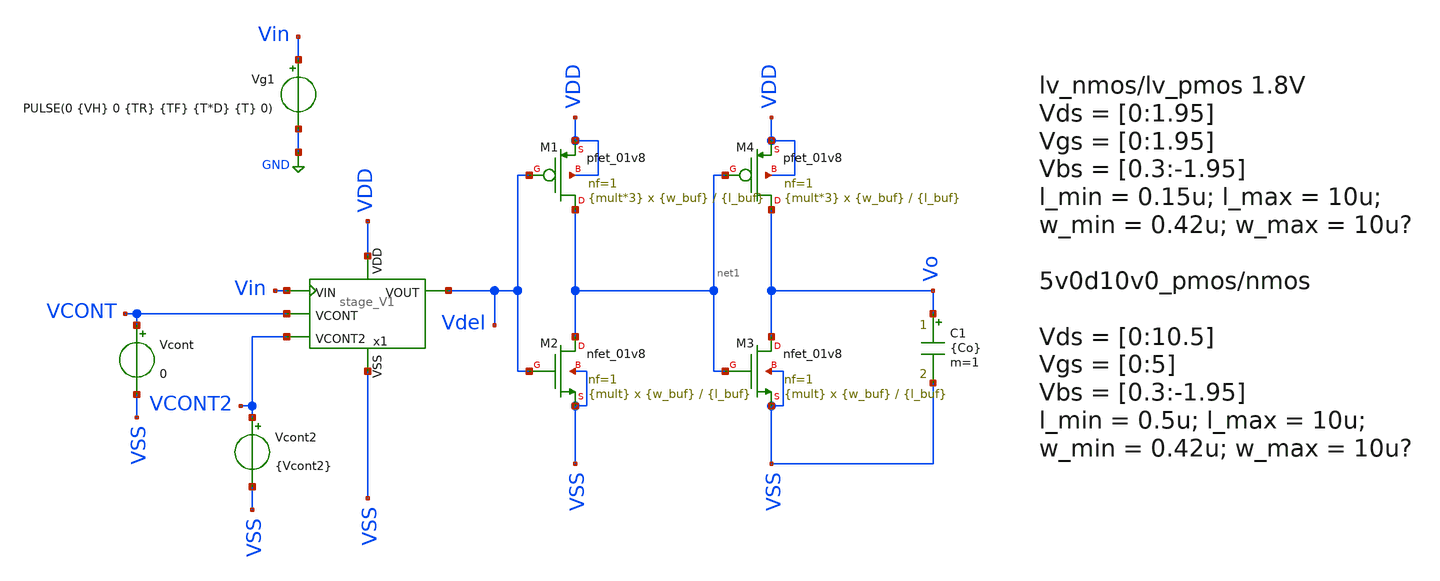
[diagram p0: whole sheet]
** sch_path: xschem/VCO/TB_DelCell_V1.sch
**.subckt TB_DelCell_V1
C1 Vo VSS {Co} m=1
Vcont VCONT VSS 0
Vg1 Vin GND PULSE(0 {VH} 0 {TR} {TF} {T*D} {T} 0)
XM2 net1 Vdel VSS VSS sky130_fd_pr__nfet_01v8 L={l_buf} W={w_buf} nf=1 ad='int((nf+1)/2) * W/nf * 0.29'
+ as='int((nf+2)/2) * W/nf * 0.29' pd='2*int((nf+1)/2) * (W/nf + 0.29)' ps='2*int((nf+2)/2) * (W/nf + 0.29)'
+ nrd='0.29 / W' nrs='0.29 / W' sa=0 sb=0 sd=0 mult={mult} m={mult}
XM1 net1 Vdel VDD VDD sky130_fd_pr__pfet_01v8 L={l_buf} W={w_buf} nf=1 ad='int((nf+1)/2) * W/nf * 0.29'
+ as='int((nf+2)/2) * W/nf * 0.29' pd='2*int((nf+1)/2) * (W/nf + 0.29)' ps='2*int((nf+2)/2) * (W/nf + 0.29)'
+ nrd='0.29 / W' nrs='0.29 / W' sa=0 sb=0 sd=0 mult={mult*3} m={mult*3}
XM3 Vo net1 VSS VSS sky130_fd_pr__nfet_01v8 L={l_buf} W={w_buf} nf=1 ad='int((nf+1)/2) * W/nf * 0.29'
+ as='int((nf+2)/2) * W/nf * 0.29' pd='2*int((nf+1)/2) * (W/nf + 0.29)' ps='2*int((nf+2)/2) * (W/nf + 0.29)'
+ nrd='0.29 / W' nrs='0.29 / W' sa=0 sb=0 sd=0 mult={mult} m={mult}
XM4 Vo net1 VDD VDD sky130_fd_pr__pfet_01v8 L={l_buf} W={w_buf} nf=1 ad='int((nf+1)/2) * W/nf * 0.29'
+ as='int((nf+2)/2) * W/nf * 0.29' pd='2*int((nf+1)/2) * (W/nf + 0.29)' ps='2*int((nf+2)/2) * (W/nf + 0.29)'
+ nrd='0.29 / W' nrs='0.29 / W' sa=0 sb=0 sd=0 mult={mult*3} m={mult*3}
x1 VDD VCONT Vdel Vin VSS VCONT2 stage_V1
Vcont2 VCONT2 VSS {Vcont2}
**** begin user architecture code

.lib /opt/pdks/sky130A/libs.tech/ngspice/sky130.lib.spice tt
*.lib /opt/pdks/sky130A/libs.tech/ngspice/sky130.lib.spice ss
*.lib /opt/pdks/sky130A/libs.tech/ngspice/sky130.lib.spice ff
*.lib /opt/pdks/sky130A/libs.tech/ngspice/sky130.lib.spice sf
*.lib /opt/pdks/sky130A/libs.tech/ngspice/sky130.lib.spice fs


.param Co = 0.1p
*.param Co = 0.1p
.param mult = 1
.param w_buf = 1
.param l_buf = 0.15

.param vvcont = 0
.param Vcont2 = 0.5

vvdd vdd 0 dc 1.8
vvss vss 0 0
*vvcont VCONT 0 dc 0
*vvcont2 VCONT2 0 dc 0
*.option temp = 200
.ic v(V_1) = 0
.ic v(V_2) = 1.8
.save v(V_1) v(Vo)


.param VH = 1.8

.ic v(Vo) = 0

*.param fsw = 10Meg
*.param fsw = 8.4Meg
*.param fsw = 1Meg
.param fsw = 50k

.param T = 1/fsw

.param D = 0.5
.param TR = 1n
.param TF = 1n
.param TdR = 0.5n
.param TdF = 0.5n

.param SimTime =  30*T
.csparam SimTime ={Simtime}
.csparam Tmargin = 10u





.save all
.tran 5n {SimTime}
.control
let Vtarg = 0.9

compose Vcont_sweep start = 0 stop = 1 step =0.1

let strt = 0
let stp = 1
let step = 0.1
let len = 1 + (stp-strt)/step

let VCN_sweep = vector(len)
let VCP_sweep = vector(len)
let Icont_sweep = vector(len)
let Iout_sweep = vector(len)
let Tdel_Sweep = vector(len)

let Index = 0

foreach val $&Vcont_sweep
	run
	alter vcont $val
	let Vo = v(Vo)
	let VCN_tran = v(x1.VCN)
	let VCP_tran = v(x1.VCP)
	let Icont_tran = i(v.x1.VIcont)
	let Iout_tran = i(v.x1.VIp)
	let In_tran  = i(v.x1.VIn)

	meas tran VCN AVG VCN_tran FROM=0 TO={SimTime}
	meas tran VCP AVG VCP_tran FROM=0 TO={SimTime}
	meas tran Icont AVG Icont_tran FROM=0 TO={SimTime}
	meas tran Iout AVG Iout_tran FROM=0 TO={SimTime}

	meas tran Tdel TRIG Vin VAL = {Vtarg} RISE = 20 TARG v(Vdel) VAL = {Vtarg}  RISE = 20

	*plot Vo Vin
	*plot VCN_tran VCP_tran
	*plot Icont_tran
	*plot Iout_tran
	print VCN VCP Icont Iout

	let VCN_sweep[index] = VCN
	let VCP_sweep[index] = VCP
	let Icont_sweep[index] = Icont
	let Iout_sweep[index] = Iout
	let Tdel_sweep[index] = Tdel
	let index = index +1
end

plot Icont_sweep vs Vcont_sweep
plot Iout_sweep vs VCP_sweep
plot Iout_sweep vs Vcont_sweep
plot VCP_sweep vs Vcont_sweep
plot Tdel_sweep vs Vcont_sweep
print VCN_sweep VCP_sweep Icont_sweep Iout_sweep Tdel_sweep

.endc




.param w_MP1a = 0.5
.param l_MP1a = 10
.param w_MP1b = 3.5
.param l_MP1b = 7
.param w_MP1 = 0.5
.param l_MP1 = 10
.param w_MP2 = 8
.param l_MP2 = 4
.param w_MP3 = 5
.param l_MP3 = 4
.param w_MP4 = 5
.param l_MP4 = 5

.param w_MN1 = 5
.param l_MN1 = 0.5
.param w_MN2 = 5
.param l_MN2 = 0.5
.param w_MN3 = 3
.param l_MN3 = 0.5
.param w_MN4 = 2
.param l_MN4 = 5



**** end user architecture code
**.ends

* expanding   symbol:  ../VCO/stage_V1.sym # of pins=6
** sym_path: xschem/VCO/stage_V1.sym
** sch_path: xschem/VCO/stage_V1.sch
.subckt stage_V1 VDD VCONT VOUT VIN VSS VCONT2
*.ipin VCONT2
*.ipin VIN
*.opin VOUT
*.iopin VDD
*.iopin VSS
*.ipin VCONT
XMN1 VSS net2 net2 VSS sg13_hv_nmos w={w_MN1} l={l_MN1} ng=1 m={m_MN1} mm_ok=1
XMN2 VSS net2 net3 VSS sg13_hv_nmos w={w_MN2} l={l_MN2} ng=1 m={m_MN2} mm_ok=1
XMN3 VSS net2 VdsMN3 VSS sg13_hv_nmos w={w_MN3} l={l_MN3} ng=1 m={m_MN3} mm_ok=1
XMP1a VCN VCONT VDD VDD sg13_hv_pmos w={w_MP1a} l={l_MP1a} ng=1 m={m_MP1a} mm_ok=1
XMP2 VCP VCP VDD VDD sg13_hv_pmos w={w_MP2} l={l_MP2} ng=1 m={m_MP2} mm_ok=1
XMP3 net4 VCP VDD VDD sg13_hv_pmos w={w_MP3} l={l_MP3} ng=1 m={m_MP3} mm_ok=1
XMP7 net1 VIN VSMP4 VDD sg13_hv_pmos w={w_MP4} l={l_MP4} ng=1 m={m_MP4} mm_ok=1
XMN4 VdsMN3 VIN net1 VSS sg13_hv_nmos w={w_MN4} l={l_MN4} ng=1 m={m_MN4} mm_ok=1
XMP1b VCN VCONT2 VDD VDD sg13_hv_pmos w={w_MP1b} l={l_MP1b} ng=1 m={m_MP1b} mm_ok=1
VIcont1 VCN net2 0
.save i(vicont1)
VIcont2 VCP net3 0
.save i(vicont2)
VIcont3 net4 VSMP4 0
.save i(vicont3)
VIcont4 net1 VOUT 0
.save i(vicont4)
.ends

.GLOBAL GND
.end
